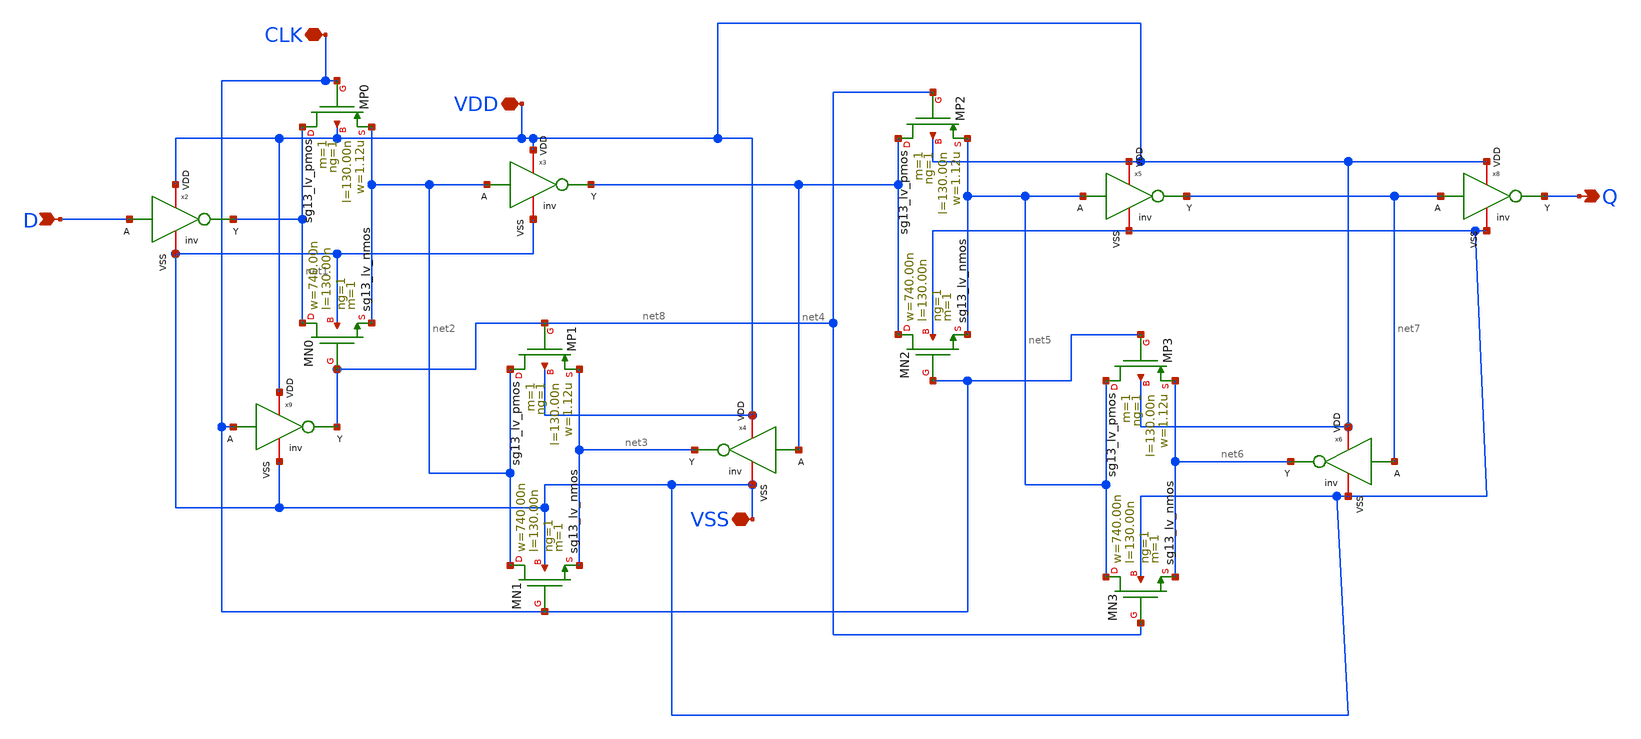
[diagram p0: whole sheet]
** sch_path: netlist/flipflop.sch
**.subckt flipflop D Q CLK VDD VSS
*.ipin D
*.opin Q
*.iopin CLK
*.iopin VDD
*.iopin VSS
XMN0 net1 net8 net2 VSS sg13_lv_nmos w=740.00n l=130.00n ng=1 m=1 mm_ok=1
XMP0 net1 CLK net2 VDD sg13_lv_pmos w=1.12u l=130.00n ng=1 m=1 mm_ok=1
XMN1 net2 CLK net3 VSS sg13_lv_nmos w=740.00n l=130.00n ng=1 m=1 mm_ok=1
XMP1 net2 net8 net3 VDD sg13_lv_pmos w=1.12u l=130.00n ng=1 m=1 mm_ok=1
x2 VDD net1 D VSS inv
x3 VDD net4 net2 VSS inv
x4 VDD net3 net4 VSS inv
XMN2 net4 CLK net5 VSS sg13_lv_nmos w=740.00n l=130.00n ng=1 m=1 mm_ok=1
XMP2 net4 net8 net5 VDD sg13_lv_pmos w=1.12u l=130.00n ng=1 m=1 mm_ok=1
XMN3 net5 net8 net6 VSS sg13_lv_nmos w=740.00n l=130.00n ng=1 m=1 mm_ok=1
XMP3 net5 CLK net6 VDD sg13_lv_pmos w=1.12u l=130.00n ng=1 m=1 mm_ok=1
x5 VDD net7 net5 VSS inv
x6 VDD net6 net7 VSS inv
x8 VDD Q net7 VSS inv
x9 VDD net8 CLK VSS inv
**.ends
.end
